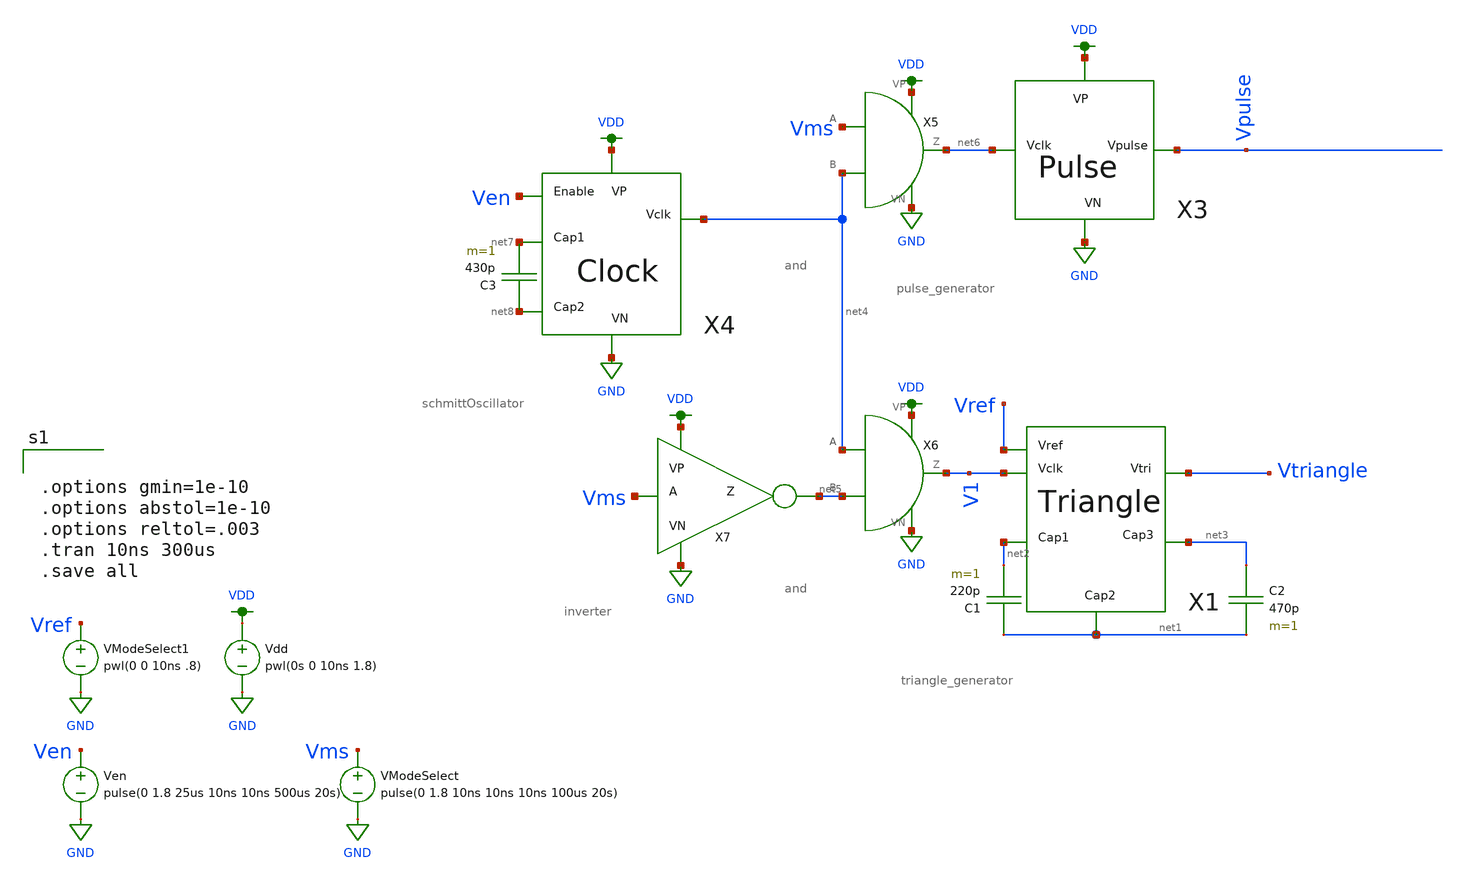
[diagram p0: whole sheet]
** sch_path: schematics/mode_select_testbench.sch
**.subckt mode_select_testbench
Vdd VDD GND pwl(0s 0 10ns 1.8)
X1 Vtriangle Vref net2 V1 net1 net3 triangle_generator
C1 net1 net2 220p m=1
C2 net3 net1 470p m=1
Ven Ven GND pulse(0 1.8 25us 10ns 10ns 500us 20s)
X3 Vpulse VDD GND net6 pulse_generator
X4 Ven net7 net8 VDD GND net4 schmittOscillator
C3 net8 net7 430p m=1
VModeSelect Vms GND pulse(0 1.8 10ns 10ns 10ns 100us 20s)
VModeSelect1 Vref GND pwl(0 0 10ns .8)
X5 Vms net4 VDD GND net6 and
X6 net4 net5 VDD GND V1 and
X7 Vms VDD GND net5 inverter
**** begin user architecture code


.options gmin=1e-10
.options abstol=1e-10
.options reltol=.003
.tran 10ns 300us
.save all


.option wnflag=1
.param MC_SWITCH=0.0
.lib ~/skywater/skywater-pdk/libraries/sky130_fd_pr_ngspice/latest/models/sky130.lib.spice tt

**** end user architecture code
**.ends
.GLOBAL GND
.GLOBAL VDD
.end
